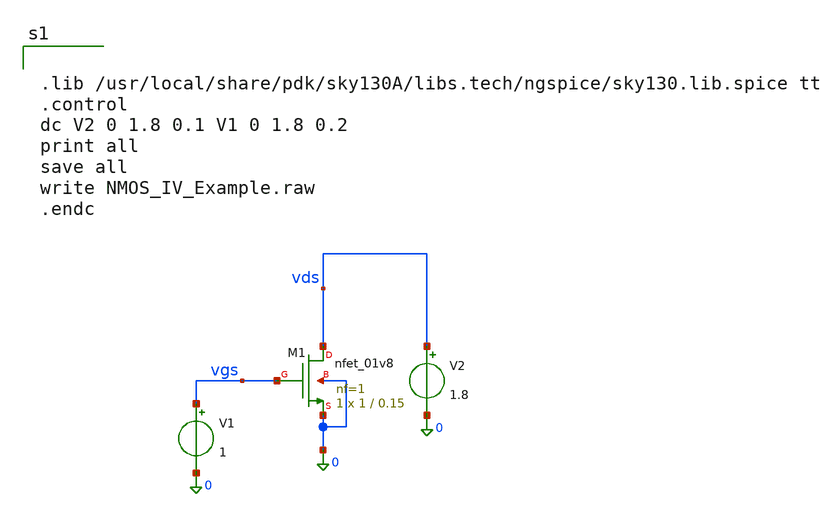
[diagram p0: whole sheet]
** sch_path: mag/layout/NMOS_IV_Example.sch
**.subckt NMOS_IV_Example
V1 vgs 0 1
V2 vds 0 1.8
XM1 vds vgs 0 0 sky130_fd_pr__nfet_01v8 L=0.15 W=1 nf=1 ad='int((1 + 1)/2) * 1 / 1 * 0.29' as='int((1 + 2)/2) * 1 / 1 * 0.29'
+ pd='2*int((1 + 1)/2) * (1 / 1 + 0.29)' ps='2*int((1 + 2)/2) * (1 / 1 + 0.29)' nrd='0.29 / 1 ' nrs='0.29 / 1 '
+ sa=0 sb=0 sd=0 mult=1 m=1
**** begin user architecture code


.lib /usr/local/share/pdk/sky130A/libs.tech/ngspice/sky130.lib.spice tt
.control
dc V2 0 1.8 0.1 V1 0 1.8 0.2
print all
save all
write NMOS_IV_Example.raw
.endc

**** end user architecture code
**.ends
.end
